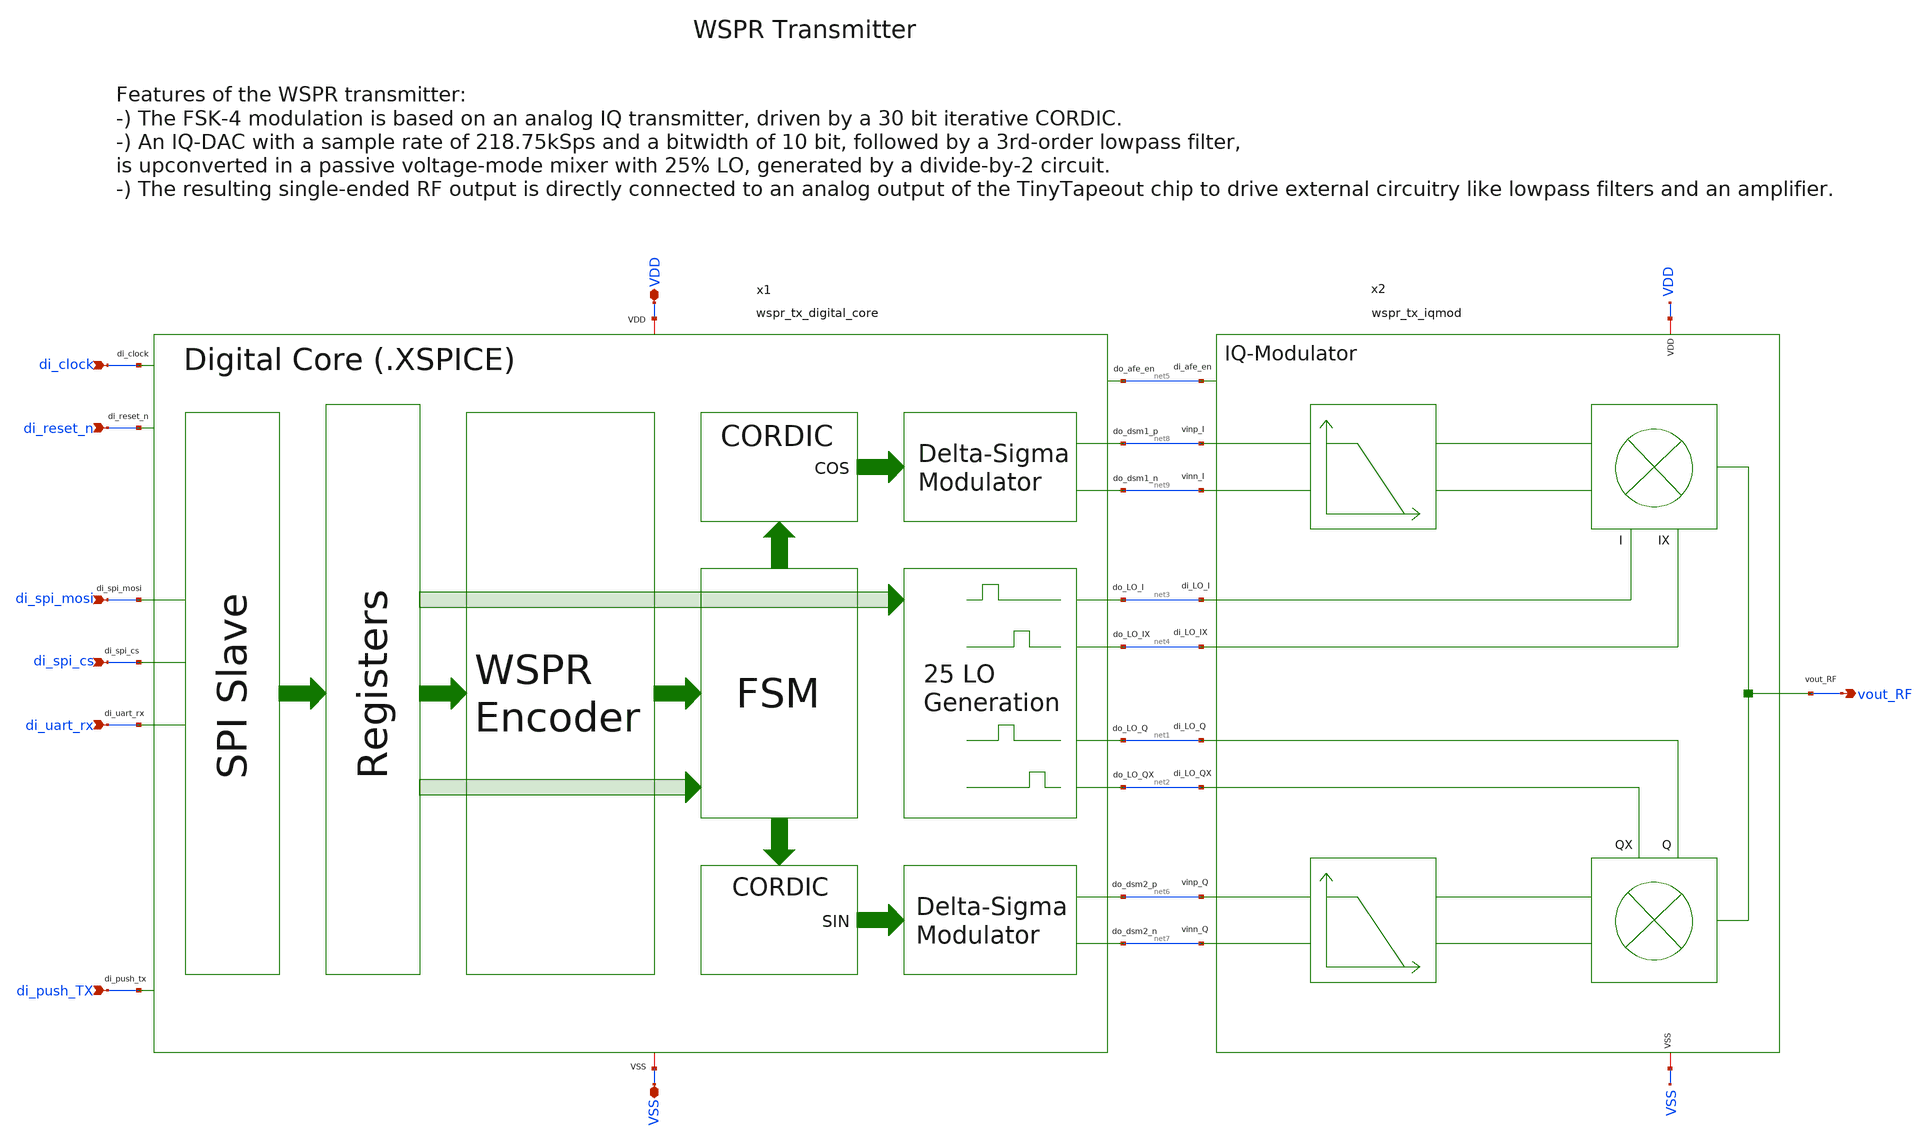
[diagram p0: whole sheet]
** sch_path: sky130/xschem/wspr_tx_top.sch
**.subckt wspr_tx_top VDD vout_RF VSS di_clock di_reset_n di_spi_mosi di_uart_rx di_push_TX
*+ di_spi_cs
*.iopin VDD
*.opin vout_RF
*.iopin VSS
*.ipin di_clock
*.ipin di_reset_n
*.ipin di_spi_mosi
*.ipin di_uart_rx
*.ipin di_push_TX
*.ipin di_spi_cs
x1 VDD VSS di_clock di_reset_n net8 net9 net7 net6 net3 net4 net1 net2 net5 di_spi_cs di_uart_rx
+ di_push_TX di_spi_mosi wspr_tx_digital_core
x2 net5 VDD net6 net7 VSS net3 net4 vout_RF net8 net9 net1 net2 wspr_tx_iqmod
**.ends
.end
